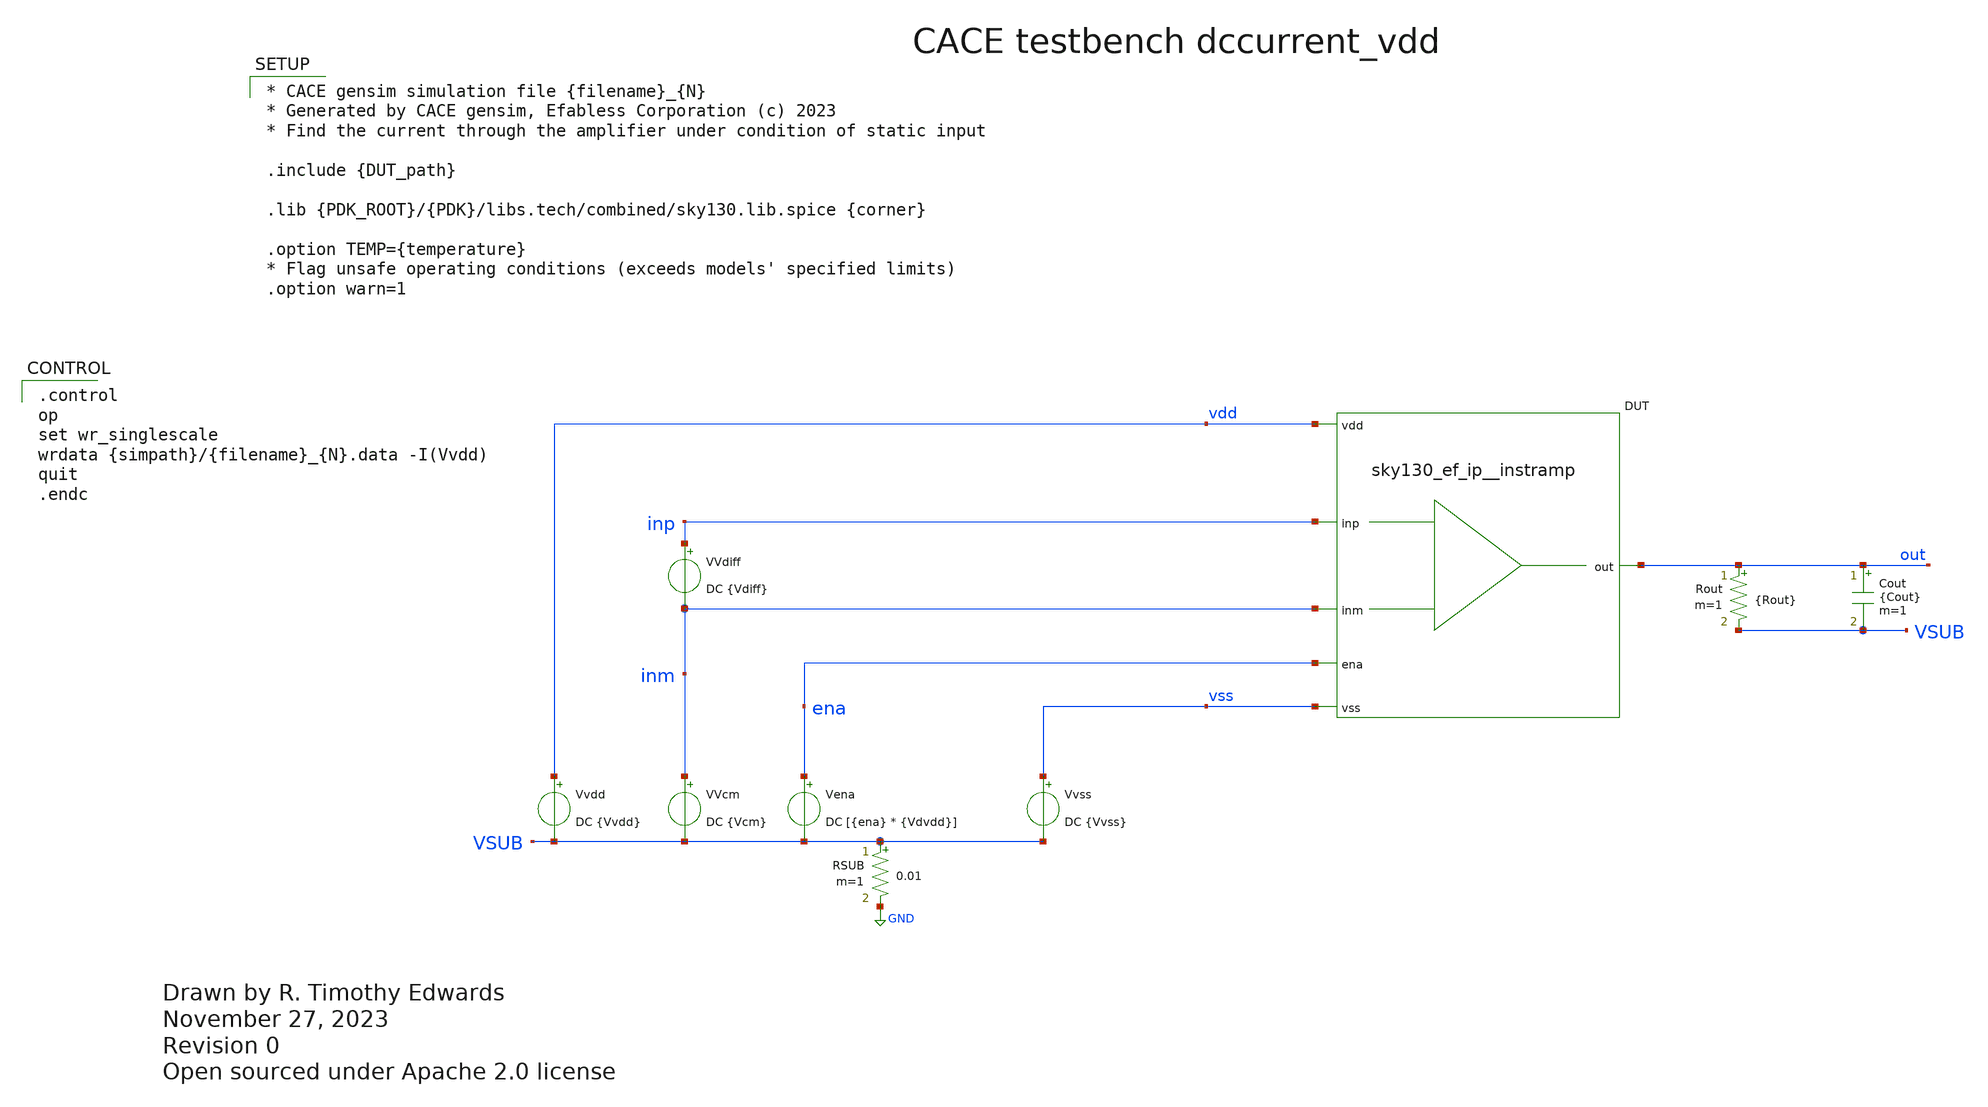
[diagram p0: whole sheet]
** sch_path: cace/dccurrent_vdd.sch
* Open sourced under Apache 2.0 license
**.subckt dccurrent_vdd
VVcm inm VSUB DC {Vcm}
Vena ena VSUB DC [{ena} * {Vdvdd}]
Vvss vss VSUB DC {Vvss}
Rout out VSUB {Rout} m=1
Cout out VSUB {Cout} m=1
Vvdd vdd VSUB DC {Vvdd}
RSUB VSUB GND 0.01 m=1
XDUT {PIN|vdd|vdd} {PIN|vss|vss} {PIN|inm|inm} {PIN|inp|inp} {PIN|out|out} {PIN|ena|ena} {DUT_name}
VVdiff inp inm DC {Vdiff}
**** begin user architecture code

.control
op
set wr_singlescale
wrdata {simpath}/{filename}_{N}.data -I(Vvdd)
quit
.endc



* CACE gensim simulation file {filename}_{N}
* Generated by CACE gensim, Efabless Corporation (c) 2023
* Find the current through the amplifier under condition of static input

.include {DUT_path}

.lib {PDK_ROOT}/{PDK}/libs.tech/combined/sky130.lib.spice {corner}

.option TEMP={temperature}
* Flag unsafe operating conditions (exceeds models' specified limits)
.option warn=1


**** end user architecture code
**.ends
.GLOBAL GND
.end
